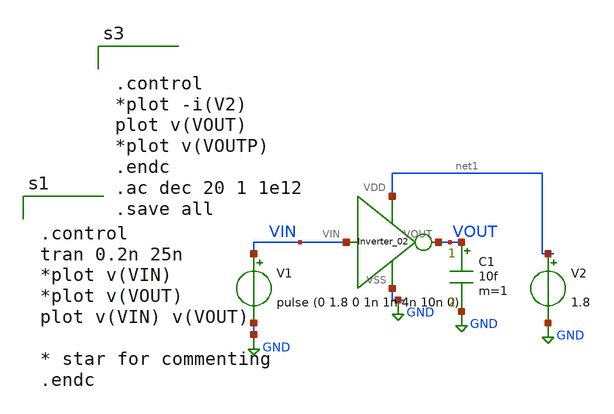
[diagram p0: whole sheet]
** sch_path: xschem/xschem_BGR_Top/Sigma_Delta/Inverter_02/Inverter_02_TB.sch
**.subckt Inverter_02_TB
V1 VIN GND pulse (0 1.8 0 1n 1n 4n 10n 0)
V2 net1 GND 1.8
C1 VOUT GND 10f m=1
X1 GND net1 VIN VOUT Inverter_02
**** begin user architecture code


.control
tran 0.2n 25n
*plot v(VIN)
*plot v(VOUT)
plot v(VIN) v(VOUT)

* star for commenting
.endc


** opencircuitdesign pdks install
.lib $::SKYWATER_MODELS/sky130.lib.spice tt




.control
*plot -i(V2)
plot v(VOUT)
*plot v(VOUTP)
.endc
.ac dec 20 1 1e12
.save all

**** end user architecture code
**.ends

* expanding   symbol:  Sigma_Delta/Inverter_02/Inverter_02.sym # of pins=4
** sym_path: xschem/xschem_BGR_Top/Sigma_Delta/Inverter_02/Inverter_02.sym
** sch_path: xschem/xschem_BGR_Top/Sigma_Delta/Inverter_02/Inverter_02.sch
.subckt Inverter_02 VSS VDD VIN VOUT
*.ipin VIN
*.iopin VDD
*.iopin VSS
*.opin VOUT
XM1 VOUT VIN VSS VSS sky130_fd_pr__nfet_01v8 L=0.15 W=0.8 nf=1 ad='int((nf+1)/2) * W/nf * 0.29' as='int((nf+2)/2) * W/nf * 0.29'
+ pd='2*int((nf+1)/2) * (W/nf + 0.29)' ps='2*int((nf+2)/2) * (W/nf + 0.29)' nrd='0.29 / W' nrs='0.29 / W'
+ sa=0 sb=0 sd=0 mult=1 m=1
XM2 VOUT VIN VDD VDD sky130_fd_pr__pfet_01v8 L=0.150 W=1.6 nf=1 ad='int((nf+1)/2) * W/nf * 0.29' as='int((nf+2)/2) * W/nf * 0.29'
+ pd='2*int((nf+1)/2) * (W/nf + 0.29)' ps='2*int((nf+2)/2) * (W/nf + 0.29)' nrd='0.29 / W' nrs='0.29 / W'
+ sa=0 sb=0 sd=0 mult=1 m=1
.ends

.GLOBAL GND
.end
